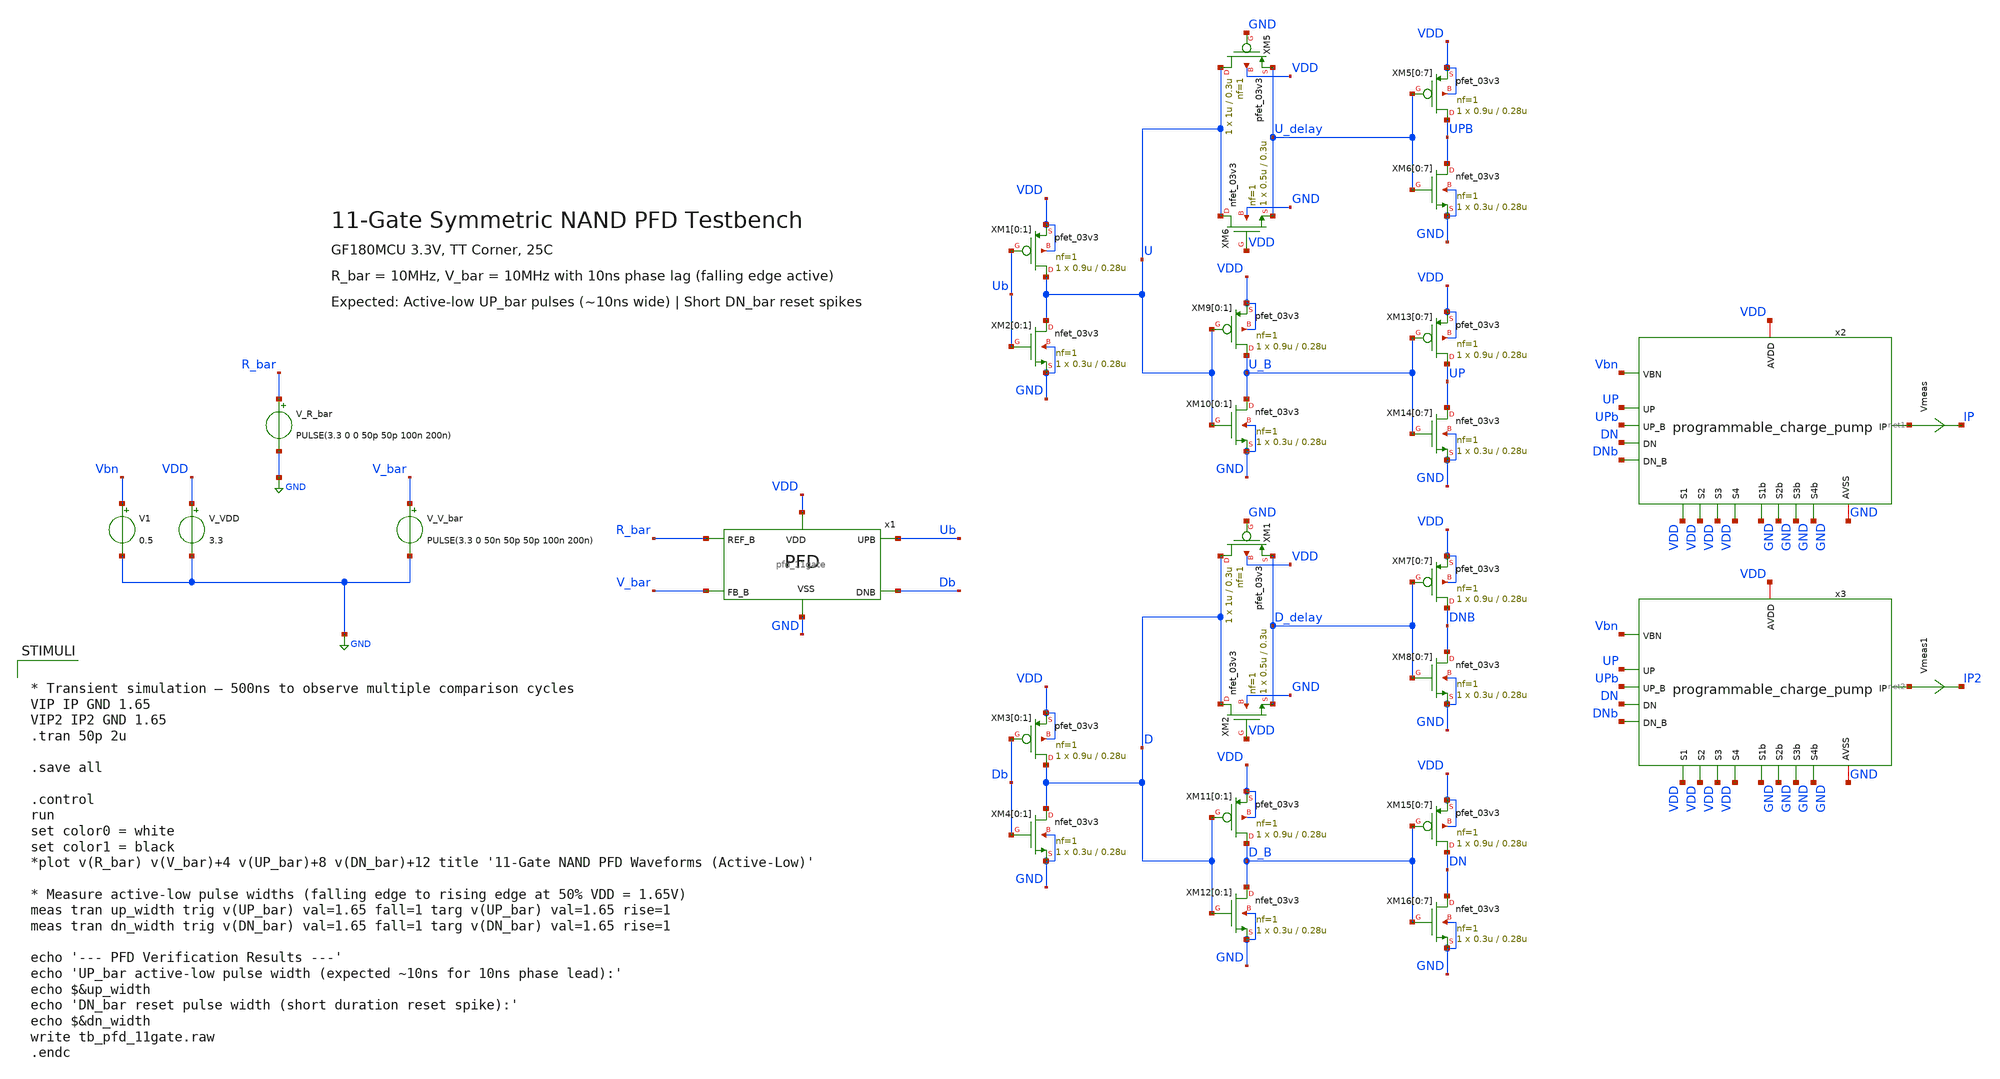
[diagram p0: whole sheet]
** sch_path: designs/libs/tb_analog/tb_pfd/tb_pfd_11gate.sch
**.subckt tb_pfd_11gate
V_R_bar R_bar GND PULSE(3.3 0 0 50p 50p 100n 200n)
V_V_bar V_bar GND PULSE(3.3 0 50n 50p 50p 100n 200n)
V_VDD VDD GND 3.3
x1 R_bar Ub Db V_bar VDD GND pfd_11gate
XM1[0] U Ub VDD VDD pfet_03v3 L=0.28u W=0.9u nf=1 ad='int((nf+1)/2) * W/nf * 0.18u' as='int((nf+2)/2) * W/nf * 0.18u'
+ pd='2*int((nf+1)/2) * (W/nf + 0.18u)' ps='2*int((nf+2)/2) * (W/nf + 0.18u)' nrd='0.18u / W' nrs='0.18u / W'
+ sa=0 sb=0 sd=0 m=1
XM1[1] U Ub VDD VDD pfet_03v3 L=0.28u W=0.9u nf=1 ad='int((nf+1)/2) * W/nf * 0.18u' as='int((nf+2)/2) * W/nf * 0.18u'
+ pd='2*int((nf+1)/2) * (W/nf + 0.18u)' ps='2*int((nf+2)/2) * (W/nf + 0.18u)' nrd='0.18u / W' nrs='0.18u / W'
+ sa=0 sb=0 sd=0 m=1
XM2[0] U Ub GND GND nfet_03v3 L=0.28u W=0.3u nf=1 ad='int((nf+1)/2) * W/nf * 0.18u' as='int((nf+2)/2) * W/nf * 0.18u'
+ pd='2*int((nf+1)/2) * (W/nf + 0.18u)' ps='2*int((nf+2)/2) * (W/nf + 0.18u)' nrd='0.18u / W' nrs='0.18u / W'
+ sa=0 sb=0 sd=0 m=1
XM2[1] U Ub GND GND nfet_03v3 L=0.28u W=0.3u nf=1 ad='int((nf+1)/2) * W/nf * 0.18u' as='int((nf+2)/2) * W/nf * 0.18u'
+ pd='2*int((nf+1)/2) * (W/nf + 0.18u)' ps='2*int((nf+2)/2) * (W/nf + 0.18u)' nrd='0.18u / W' nrs='0.18u / W'
+ sa=0 sb=0 sd=0 m=1
XM5 U GND U_delay VDD pfet_03v3 L=0.3u W=1u nf=1 ad='int((nf+1)/2) * W/nf * 0.18u' as='int((nf+2)/2) * W/nf * 0.18u'
+ pd='2*int((nf+1)/2) * (W/nf + 0.18u)' ps='2*int((nf+2)/2) * (W/nf + 0.18u)' nrd='0.18u / W' nrs='0.18u / W'
+ sa=0 sb=0 sd=0 m=1
XM6 U VDD U_delay GND nfet_03v3 L=0.3u W=0.5u nf=1 ad='int((nf+1)/2) * W/nf * 0.18u' as='int((nf+2)/2) * W/nf * 0.18u'
+ pd='2*int((nf+1)/2) * (W/nf + 0.18u)' ps='2*int((nf+2)/2) * (W/nf + 0.18u)' nrd='0.18u / W' nrs='0.18u / W'
+ sa=0 sb=0 sd=0 m=1
x2 GND VDD UP UPb DN net1 DNb Vbn GND VDD GND VDD GND VDD GND VDD programmable_charge_pump
V1 Vbn GND 0.5
Vmeas net1 IP 0
.save i(vmeas)
x3 GND VDD UP UPb DN net2 DNb Vbn GND VDD GND VDD GND VDD GND VDD programmable_charge_pump
Vmeas1 net2 IP2 0
.save i(vmeas1)
XM5[0] UPB U_delay VDD VDD pfet_03v3 L=0.28u W=0.9u nf=1 ad='int((nf+1)/2) * W/nf * 0.18u' as='int((nf+2)/2) * W/nf * 0.18u'
+ pd='2*int((nf+1)/2) * (W/nf + 0.18u)' ps='2*int((nf+2)/2) * (W/nf + 0.18u)' nrd='0.18u / W' nrs='0.18u / W'
+ sa=0 sb=0 sd=0 m=1
XM5[1] UPB U_delay VDD VDD pfet_03v3 L=0.28u W=0.9u nf=1 ad='int((nf+1)/2) * W/nf * 0.18u' as='int((nf+2)/2) * W/nf * 0.18u'
+ pd='2*int((nf+1)/2) * (W/nf + 0.18u)' ps='2*int((nf+2)/2) * (W/nf + 0.18u)' nrd='0.18u / W' nrs='0.18u / W'
+ sa=0 sb=0 sd=0 m=1
XM5[2] UPB U_delay VDD VDD pfet_03v3 L=0.28u W=0.9u nf=1 ad='int((nf+1)/2) * W/nf * 0.18u' as='int((nf+2)/2) * W/nf * 0.18u'
+ pd='2*int((nf+1)/2) * (W/nf + 0.18u)' ps='2*int((nf+2)/2) * (W/nf + 0.18u)' nrd='0.18u / W' nrs='0.18u / W'
+ sa=0 sb=0 sd=0 m=1
XM5[3] UPB U_delay VDD VDD pfet_03v3 L=0.28u W=0.9u nf=1 ad='int((nf+1)/2) * W/nf * 0.18u' as='int((nf+2)/2) * W/nf * 0.18u'
+ pd='2*int((nf+1)/2) * (W/nf + 0.18u)' ps='2*int((nf+2)/2) * (W/nf + 0.18u)' nrd='0.18u / W' nrs='0.18u / W'
+ sa=0 sb=0 sd=0 m=1
XM5[4] UPB U_delay VDD VDD pfet_03v3 L=0.28u W=0.9u nf=1 ad='int((nf+1)/2) * W/nf * 0.18u' as='int((nf+2)/2) * W/nf * 0.18u'
+ pd='2*int((nf+1)/2) * (W/nf + 0.18u)' ps='2*int((nf+2)/2) * (W/nf + 0.18u)' nrd='0.18u / W' nrs='0.18u / W'
+ sa=0 sb=0 sd=0 m=1
XM5[5] UPB U_delay VDD VDD pfet_03v3 L=0.28u W=0.9u nf=1 ad='int((nf+1)/2) * W/nf * 0.18u' as='int((nf+2)/2) * W/nf * 0.18u'
+ pd='2*int((nf+1)/2) * (W/nf + 0.18u)' ps='2*int((nf+2)/2) * (W/nf + 0.18u)' nrd='0.18u / W' nrs='0.18u / W'
+ sa=0 sb=0 sd=0 m=1
XM5[6] UPB U_delay VDD VDD pfet_03v3 L=0.28u W=0.9u nf=1 ad='int((nf+1)/2) * W/nf * 0.18u' as='int((nf+2)/2) * W/nf * 0.18u'
+ pd='2*int((nf+1)/2) * (W/nf + 0.18u)' ps='2*int((nf+2)/2) * (W/nf + 0.18u)' nrd='0.18u / W' nrs='0.18u / W'
+ sa=0 sb=0 sd=0 m=1
XM5[7] UPB U_delay VDD VDD pfet_03v3 L=0.28u W=0.9u nf=1 ad='int((nf+1)/2) * W/nf * 0.18u' as='int((nf+2)/2) * W/nf * 0.18u'
+ pd='2*int((nf+1)/2) * (W/nf + 0.18u)' ps='2*int((nf+2)/2) * (W/nf + 0.18u)' nrd='0.18u / W' nrs='0.18u / W'
+ sa=0 sb=0 sd=0 m=1
XM6[0] UPB U_delay GND GND nfet_03v3 L=0.28u W=0.3u nf=1 ad='int((nf+1)/2) * W/nf * 0.18u' as='int((nf+2)/2) * W/nf * 0.18u'
+ pd='2*int((nf+1)/2) * (W/nf + 0.18u)' ps='2*int((nf+2)/2) * (W/nf + 0.18u)' nrd='0.18u / W' nrs='0.18u / W'
+ sa=0 sb=0 sd=0 m=1
XM6[1] UPB U_delay GND GND nfet_03v3 L=0.28u W=0.3u nf=1 ad='int((nf+1)/2) * W/nf * 0.18u' as='int((nf+2)/2) * W/nf * 0.18u'
+ pd='2*int((nf+1)/2) * (W/nf + 0.18u)' ps='2*int((nf+2)/2) * (W/nf + 0.18u)' nrd='0.18u / W' nrs='0.18u / W'
+ sa=0 sb=0 sd=0 m=1
XM6[2] UPB U_delay GND GND nfet_03v3 L=0.28u W=0.3u nf=1 ad='int((nf+1)/2) * W/nf * 0.18u' as='int((nf+2)/2) * W/nf * 0.18u'
+ pd='2*int((nf+1)/2) * (W/nf + 0.18u)' ps='2*int((nf+2)/2) * (W/nf + 0.18u)' nrd='0.18u / W' nrs='0.18u / W'
+ sa=0 sb=0 sd=0 m=1
XM6[3] UPB U_delay GND GND nfet_03v3 L=0.28u W=0.3u nf=1 ad='int((nf+1)/2) * W/nf * 0.18u' as='int((nf+2)/2) * W/nf * 0.18u'
+ pd='2*int((nf+1)/2) * (W/nf + 0.18u)' ps='2*int((nf+2)/2) * (W/nf + 0.18u)' nrd='0.18u / W' nrs='0.18u / W'
+ sa=0 sb=0 sd=0 m=1
XM6[4] UPB U_delay GND GND nfet_03v3 L=0.28u W=0.3u nf=1 ad='int((nf+1)/2) * W/nf * 0.18u' as='int((nf+2)/2) * W/nf * 0.18u'
+ pd='2*int((nf+1)/2) * (W/nf + 0.18u)' ps='2*int((nf+2)/2) * (W/nf + 0.18u)' nrd='0.18u / W' nrs='0.18u / W'
+ sa=0 sb=0 sd=0 m=1
XM6[5] UPB U_delay GND GND nfet_03v3 L=0.28u W=0.3u nf=1 ad='int((nf+1)/2) * W/nf * 0.18u' as='int((nf+2)/2) * W/nf * 0.18u'
+ pd='2*int((nf+1)/2) * (W/nf + 0.18u)' ps='2*int((nf+2)/2) * (W/nf + 0.18u)' nrd='0.18u / W' nrs='0.18u / W'
+ sa=0 sb=0 sd=0 m=1
XM6[6] UPB U_delay GND GND nfet_03v3 L=0.28u W=0.3u nf=1 ad='int((nf+1)/2) * W/nf * 0.18u' as='int((nf+2)/2) * W/nf * 0.18u'
+ pd='2*int((nf+1)/2) * (W/nf + 0.18u)' ps='2*int((nf+2)/2) * (W/nf + 0.18u)' nrd='0.18u / W' nrs='0.18u / W'
+ sa=0 sb=0 sd=0 m=1
XM6[7] UPB U_delay GND GND nfet_03v3 L=0.28u W=0.3u nf=1 ad='int((nf+1)/2) * W/nf * 0.18u' as='int((nf+2)/2) * W/nf * 0.18u'
+ pd='2*int((nf+1)/2) * (W/nf + 0.18u)' ps='2*int((nf+2)/2) * (W/nf + 0.18u)' nrd='0.18u / W' nrs='0.18u / W'
+ sa=0 sb=0 sd=0 m=1
XM9[0] U_B U VDD VDD pfet_03v3 L=0.28u W=0.9u nf=1 ad='int((nf+1)/2) * W/nf * 0.18u' as='int((nf+2)/2) * W/nf * 0.18u'
+ pd='2*int((nf+1)/2) * (W/nf + 0.18u)' ps='2*int((nf+2)/2) * (W/nf + 0.18u)' nrd='0.18u / W' nrs='0.18u / W'
+ sa=0 sb=0 sd=0 m=1
XM9[1] U_B U VDD VDD pfet_03v3 L=0.28u W=0.9u nf=1 ad='int((nf+1)/2) * W/nf * 0.18u' as='int((nf+2)/2) * W/nf * 0.18u'
+ pd='2*int((nf+1)/2) * (W/nf + 0.18u)' ps='2*int((nf+2)/2) * (W/nf + 0.18u)' nrd='0.18u / W' nrs='0.18u / W'
+ sa=0 sb=0 sd=0 m=1
XM10[0] U_B U GND GND nfet_03v3 L=0.28u W=0.3u nf=1 ad='int((nf+1)/2) * W/nf * 0.18u' as='int((nf+2)/2) * W/nf * 0.18u'
+ pd='2*int((nf+1)/2) * (W/nf + 0.18u)' ps='2*int((nf+2)/2) * (W/nf + 0.18u)' nrd='0.18u / W' nrs='0.18u / W'
+ sa=0 sb=0 sd=0 m=1
XM10[1] U_B U GND GND nfet_03v3 L=0.28u W=0.3u nf=1 ad='int((nf+1)/2) * W/nf * 0.18u' as='int((nf+2)/2) * W/nf * 0.18u'
+ pd='2*int((nf+1)/2) * (W/nf + 0.18u)' ps='2*int((nf+2)/2) * (W/nf + 0.18u)' nrd='0.18u / W' nrs='0.18u / W'
+ sa=0 sb=0 sd=0 m=1
XM13[0] UP U_B VDD VDD pfet_03v3 L=0.28u W=0.9u nf=1 ad='int((nf+1)/2) * W/nf * 0.18u' as='int((nf+2)/2) * W/nf * 0.18u'
+ pd='2*int((nf+1)/2) * (W/nf + 0.18u)' ps='2*int((nf+2)/2) * (W/nf + 0.18u)' nrd='0.18u / W' nrs='0.18u / W'
+ sa=0 sb=0 sd=0 m=1
XM13[1] UP U_B VDD VDD pfet_03v3 L=0.28u W=0.9u nf=1 ad='int((nf+1)/2) * W/nf * 0.18u' as='int((nf+2)/2) * W/nf * 0.18u'
+ pd='2*int((nf+1)/2) * (W/nf + 0.18u)' ps='2*int((nf+2)/2) * (W/nf + 0.18u)' nrd='0.18u / W' nrs='0.18u / W'
+ sa=0 sb=0 sd=0 m=1
XM13[2] UP U_B VDD VDD pfet_03v3 L=0.28u W=0.9u nf=1 ad='int((nf+1)/2) * W/nf * 0.18u' as='int((nf+2)/2) * W/nf * 0.18u'
+ pd='2*int((nf+1)/2) * (W/nf + 0.18u)' ps='2*int((nf+2)/2) * (W/nf + 0.18u)' nrd='0.18u / W' nrs='0.18u / W'
+ sa=0 sb=0 sd=0 m=1
XM13[3] UP U_B VDD VDD pfet_03v3 L=0.28u W=0.9u nf=1 ad='int((nf+1)/2) * W/nf * 0.18u' as='int((nf+2)/2) * W/nf * 0.18u'
+ pd='2*int((nf+1)/2) * (W/nf + 0.18u)' ps='2*int((nf+2)/2) * (W/nf + 0.18u)' nrd='0.18u / W' nrs='0.18u / W'
+ sa=0 sb=0 sd=0 m=1
XM13[4] UP U_B VDD VDD pfet_03v3 L=0.28u W=0.9u nf=1 ad='int((nf+1)/2) * W/nf * 0.18u' as='int((nf+2)/2) * W/nf * 0.18u'
+ pd='2*int((nf+1)/2) * (W/nf + 0.18u)' ps='2*int((nf+2)/2) * (W/nf + 0.18u)' nrd='0.18u / W' nrs='0.18u / W'
+ sa=0 sb=0 sd=0 m=1
XM13[5] UP U_B VDD VDD pfet_03v3 L=0.28u W=0.9u nf=1 ad='int((nf+1)/2) * W/nf * 0.18u' as='int((nf+2)/2) * W/nf * 0.18u'
+ pd='2*int((nf+1)/2) * (W/nf + 0.18u)' ps='2*int((nf+2)/2) * (W/nf + 0.18u)' nrd='0.18u / W' nrs='0.18u / W'
+ sa=0 sb=0 sd=0 m=1
XM13[6] UP U_B VDD VDD pfet_03v3 L=0.28u W=0.9u nf=1 ad='int((nf+1)/2) * W/nf * 0.18u' as='int((nf+2)/2) * W/nf * 0.18u'
+ pd='2*int((nf+1)/2) * (W/nf + 0.18u)' ps='2*int((nf+2)/2) * (W/nf + 0.18u)' nrd='0.18u / W' nrs='0.18u / W'
+ sa=0 sb=0 sd=0 m=1
XM13[7] UP U_B VDD VDD pfet_03v3 L=0.28u W=0.9u nf=1 ad='int((nf+1)/2) * W/nf * 0.18u' as='int((nf+2)/2) * W/nf * 0.18u'
+ pd='2*int((nf+1)/2) * (W/nf + 0.18u)' ps='2*int((nf+2)/2) * (W/nf + 0.18u)' nrd='0.18u / W' nrs='0.18u / W'
+ sa=0 sb=0 sd=0 m=1
XM14[0] UP U_B GND GND nfet_03v3 L=0.28u W=0.3u nf=1 ad='int((nf+1)/2) * W/nf * 0.18u' as='int((nf+2)/2) * W/nf * 0.18u'
+ pd='2*int((nf+1)/2) * (W/nf + 0.18u)' ps='2*int((nf+2)/2) * (W/nf + 0.18u)' nrd='0.18u / W' nrs='0.18u / W'
+ sa=0 sb=0 sd=0 m=1
XM14[1] UP U_B GND GND nfet_03v3 L=0.28u W=0.3u nf=1 ad='int((nf+1)/2) * W/nf * 0.18u' as='int((nf+2)/2) * W/nf * 0.18u'
+ pd='2*int((nf+1)/2) * (W/nf + 0.18u)' ps='2*int((nf+2)/2) * (W/nf + 0.18u)' nrd='0.18u / W' nrs='0.18u / W'
+ sa=0 sb=0 sd=0 m=1
XM14[2] UP U_B GND GND nfet_03v3 L=0.28u W=0.3u nf=1 ad='int((nf+1)/2) * W/nf * 0.18u' as='int((nf+2)/2) * W/nf * 0.18u'
+ pd='2*int((nf+1)/2) * (W/nf + 0.18u)' ps='2*int((nf+2)/2) * (W/nf + 0.18u)' nrd='0.18u / W' nrs='0.18u / W'
+ sa=0 sb=0 sd=0 m=1
XM14[3] UP U_B GND GND nfet_03v3 L=0.28u W=0.3u nf=1 ad='int((nf+1)/2) * W/nf * 0.18u' as='int((nf+2)/2) * W/nf * 0.18u'
+ pd='2*int((nf+1)/2) * (W/nf + 0.18u)' ps='2*int((nf+2)/2) * (W/nf + 0.18u)' nrd='0.18u / W' nrs='0.18u / W'
+ sa=0 sb=0 sd=0 m=1
XM14[4] UP U_B GND GND nfet_03v3 L=0.28u W=0.3u nf=1 ad='int((nf+1)/2) * W/nf * 0.18u' as='int((nf+2)/2) * W/nf * 0.18u'
+ pd='2*int((nf+1)/2) * (W/nf + 0.18u)' ps='2*int((nf+2)/2) * (W/nf + 0.18u)' nrd='0.18u / W' nrs='0.18u / W'
+ sa=0 sb=0 sd=0 m=1
XM14[5] UP U_B GND GND nfet_03v3 L=0.28u W=0.3u nf=1 ad='int((nf+1)/2) * W/nf * 0.18u' as='int((nf+2)/2) * W/nf * 0.18u'
+ pd='2*int((nf+1)/2) * (W/nf + 0.18u)' ps='2*int((nf+2)/2) * (W/nf + 0.18u)' nrd='0.18u / W' nrs='0.18u / W'
+ sa=0 sb=0 sd=0 m=1
XM14[6] UP U_B GND GND nfet_03v3 L=0.28u W=0.3u nf=1 ad='int((nf+1)/2) * W/nf * 0.18u' as='int((nf+2)/2) * W/nf * 0.18u'
+ pd='2*int((nf+1)/2) * (W/nf + 0.18u)' ps='2*int((nf+2)/2) * (W/nf + 0.18u)' nrd='0.18u / W' nrs='0.18u / W'
+ sa=0 sb=0 sd=0 m=1
XM14[7] UP U_B GND GND nfet_03v3 L=0.28u W=0.3u nf=1 ad='int((nf+1)/2) * W/nf * 0.18u' as='int((nf+2)/2) * W/nf * 0.18u'
+ pd='2*int((nf+1)/2) * (W/nf + 0.18u)' ps='2*int((nf+2)/2) * (W/nf + 0.18u)' nrd='0.18u / W' nrs='0.18u / W'
+ sa=0 sb=0 sd=0 m=1
XM3[0] D Db VDD VDD pfet_03v3 L=0.28u W=0.9u nf=1 ad='int((nf+1)/2) * W/nf * 0.18u' as='int((nf+2)/2) * W/nf * 0.18u'
+ pd='2*int((nf+1)/2) * (W/nf + 0.18u)' ps='2*int((nf+2)/2) * (W/nf + 0.18u)' nrd='0.18u / W' nrs='0.18u / W'
+ sa=0 sb=0 sd=0 m=1
XM3[1] D Db VDD VDD pfet_03v3 L=0.28u W=0.9u nf=1 ad='int((nf+1)/2) * W/nf * 0.18u' as='int((nf+2)/2) * W/nf * 0.18u'
+ pd='2*int((nf+1)/2) * (W/nf + 0.18u)' ps='2*int((nf+2)/2) * (W/nf + 0.18u)' nrd='0.18u / W' nrs='0.18u / W'
+ sa=0 sb=0 sd=0 m=1
XM4[0] D Db GND GND nfet_03v3 L=0.28u W=0.3u nf=1 ad='int((nf+1)/2) * W/nf * 0.18u' as='int((nf+2)/2) * W/nf * 0.18u'
+ pd='2*int((nf+1)/2) * (W/nf + 0.18u)' ps='2*int((nf+2)/2) * (W/nf + 0.18u)' nrd='0.18u / W' nrs='0.18u / W'
+ sa=0 sb=0 sd=0 m=1
XM4[1] D Db GND GND nfet_03v3 L=0.28u W=0.3u nf=1 ad='int((nf+1)/2) * W/nf * 0.18u' as='int((nf+2)/2) * W/nf * 0.18u'
+ pd='2*int((nf+1)/2) * (W/nf + 0.18u)' ps='2*int((nf+2)/2) * (W/nf + 0.18u)' nrd='0.18u / W' nrs='0.18u / W'
+ sa=0 sb=0 sd=0 m=1
XM7[0] DNB D_delay VDD VDD pfet_03v3 L=0.28u W=0.9u nf=1 ad='int((nf+1)/2) * W/nf * 0.18u' as='int((nf+2)/2) * W/nf * 0.18u'
+ pd='2*int((nf+1)/2) * (W/nf + 0.18u)' ps='2*int((nf+2)/2) * (W/nf + 0.18u)' nrd='0.18u / W' nrs='0.18u / W'
+ sa=0 sb=0 sd=0 m=1
XM7[1] DNB D_delay VDD VDD pfet_03v3 L=0.28u W=0.9u nf=1 ad='int((nf+1)/2) * W/nf * 0.18u' as='int((nf+2)/2) * W/nf * 0.18u'
+ pd='2*int((nf+1)/2) * (W/nf + 0.18u)' ps='2*int((nf+2)/2) * (W/nf + 0.18u)' nrd='0.18u / W' nrs='0.18u / W'
+ sa=0 sb=0 sd=0 m=1
XM7[2] DNB D_delay VDD VDD pfet_03v3 L=0.28u W=0.9u nf=1 ad='int((nf+1)/2) * W/nf * 0.18u' as='int((nf+2)/2) * W/nf * 0.18u'
+ pd='2*int((nf+1)/2) * (W/nf + 0.18u)' ps='2*int((nf+2)/2) * (W/nf + 0.18u)' nrd='0.18u / W' nrs='0.18u / W'
+ sa=0 sb=0 sd=0 m=1
XM7[3] DNB D_delay VDD VDD pfet_03v3 L=0.28u W=0.9u nf=1 ad='int((nf+1)/2) * W/nf * 0.18u' as='int((nf+2)/2) * W/nf * 0.18u'
+ pd='2*int((nf+1)/2) * (W/nf + 0.18u)' ps='2*int((nf+2)/2) * (W/nf + 0.18u)' nrd='0.18u / W' nrs='0.18u / W'
+ sa=0 sb=0 sd=0 m=1
XM7[4] DNB D_delay VDD VDD pfet_03v3 L=0.28u W=0.9u nf=1 ad='int((nf+1)/2) * W/nf * 0.18u' as='int((nf+2)/2) * W/nf * 0.18u'
+ pd='2*int((nf+1)/2) * (W/nf + 0.18u)' ps='2*int((nf+2)/2) * (W/nf + 0.18u)' nrd='0.18u / W' nrs='0.18u / W'
+ sa=0 sb=0 sd=0 m=1
XM7[5] DNB D_delay VDD VDD pfet_03v3 L=0.28u W=0.9u nf=1 ad='int((nf+1)/2) * W/nf * 0.18u' as='int((nf+2)/2) * W/nf * 0.18u'
+ pd='2*int((nf+1)/2) * (W/nf + 0.18u)' ps='2*int((nf+2)/2) * (W/nf + 0.18u)' nrd='0.18u / W' nrs='0.18u / W'
+ sa=0 sb=0 sd=0 m=1
XM7[6] DNB D_delay VDD VDD pfet_03v3 L=0.28u W=0.9u nf=1 ad='int((nf+1)/2) * W/nf * 0.18u' as='int((nf+2)/2) * W/nf * 0.18u'
+ pd='2*int((nf+1)/2) * (W/nf + 0.18u)' ps='2*int((nf+2)/2) * (W/nf + 0.18u)' nrd='0.18u / W' nrs='0.18u / W'
+ sa=0 sb=0 sd=0 m=1
XM7[7] DNB D_delay VDD VDD pfet_03v3 L=0.28u W=0.9u nf=1 ad='int((nf+1)/2) * W/nf * 0.18u' as='int((nf+2)/2) * W/nf * 0.18u'
+ pd='2*int((nf+1)/2) * (W/nf + 0.18u)' ps='2*int((nf+2)/2) * (W/nf + 0.18u)' nrd='0.18u / W' nrs='0.18u / W'
+ sa=0 sb=0 sd=0 m=1
XM8[0] DNB D_delay GND GND nfet_03v3 L=0.28u W=0.3u nf=1 ad='int((nf+1)/2) * W/nf * 0.18u' as='int((nf+2)/2) * W/nf * 0.18u'
+ pd='2*int((nf+1)/2) * (W/nf + 0.18u)' ps='2*int((nf+2)/2) * (W/nf + 0.18u)' nrd='0.18u / W' nrs='0.18u / W'
+ sa=0 sb=0 sd=0 m=1
XM8[1] DNB D_delay GND GND nfet_03v3 L=0.28u W=0.3u nf=1 ad='int((nf+1)/2) * W/nf * 0.18u' as='int((nf+2)/2) * W/nf * 0.18u'
+ pd='2*int((nf+1)/2) * (W/nf + 0.18u)' ps='2*int((nf+2)/2) * (W/nf + 0.18u)' nrd='0.18u / W' nrs='0.18u / W'
+ sa=0 sb=0 sd=0 m=1
XM8[2] DNB D_delay GND GND nfet_03v3 L=0.28u W=0.3u nf=1 ad='int((nf+1)/2) * W/nf * 0.18u' as='int((nf+2)/2) * W/nf * 0.18u'
+ pd='2*int((nf+1)/2) * (W/nf + 0.18u)' ps='2*int((nf+2)/2) * (W/nf + 0.18u)' nrd='0.18u / W' nrs='0.18u / W'
+ sa=0 sb=0 sd=0 m=1
XM8[3] DNB D_delay GND GND nfet_03v3 L=0.28u W=0.3u nf=1 ad='int((nf+1)/2) * W/nf * 0.18u' as='int((nf+2)/2) * W/nf * 0.18u'
+ pd='2*int((nf+1)/2) * (W/nf + 0.18u)' ps='2*int((nf+2)/2) * (W/nf + 0.18u)' nrd='0.18u / W' nrs='0.18u / W'
+ sa=0 sb=0 sd=0 m=1
XM8[4] DNB D_delay GND GND nfet_03v3 L=0.28u W=0.3u nf=1 ad='int((nf+1)/2) * W/nf * 0.18u' as='int((nf+2)/2) * W/nf * 0.18u'
+ pd='2*int((nf+1)/2) * (W/nf + 0.18u)' ps='2*int((nf+2)/2) * (W/nf + 0.18u)' nrd='0.18u / W' nrs='0.18u / W'
+ sa=0 sb=0 sd=0 m=1
XM8[5] DNB D_delay GND GND nfet_03v3 L=0.28u W=0.3u nf=1 ad='int((nf+1)/2) * W/nf * 0.18u' as='int((nf+2)/2) * W/nf * 0.18u'
+ pd='2*int((nf+1)/2) * (W/nf + 0.18u)' ps='2*int((nf+2)/2) * (W/nf + 0.18u)' nrd='0.18u / W' nrs='0.18u / W'
+ sa=0 sb=0 sd=0 m=1
XM8[6] DNB D_delay GND GND nfet_03v3 L=0.28u W=0.3u nf=1 ad='int((nf+1)/2) * W/nf * 0.18u' as='int((nf+2)/2) * W/nf * 0.18u'
+ pd='2*int((nf+1)/2) * (W/nf + 0.18u)' ps='2*int((nf+2)/2) * (W/nf + 0.18u)' nrd='0.18u / W' nrs='0.18u / W'
+ sa=0 sb=0 sd=0 m=1
XM8[7] DNB D_delay GND GND nfet_03v3 L=0.28u W=0.3u nf=1 ad='int((nf+1)/2) * W/nf * 0.18u' as='int((nf+2)/2) * W/nf * 0.18u'
+ pd='2*int((nf+1)/2) * (W/nf + 0.18u)' ps='2*int((nf+2)/2) * (W/nf + 0.18u)' nrd='0.18u / W' nrs='0.18u / W'
+ sa=0 sb=0 sd=0 m=1
XM11[0] D_B D VDD VDD pfet_03v3 L=0.28u W=0.9u nf=1 ad='int((nf+1)/2) * W/nf * 0.18u' as='int((nf+2)/2) * W/nf * 0.18u'
+ pd='2*int((nf+1)/2) * (W/nf + 0.18u)' ps='2*int((nf+2)/2) * (W/nf + 0.18u)' nrd='0.18u / W' nrs='0.18u / W'
+ sa=0 sb=0 sd=0 m=1
XM11[1] D_B D VDD VDD pfet_03v3 L=0.28u W=0.9u nf=1 ad='int((nf+1)/2) * W/nf * 0.18u' as='int((nf+2)/2) * W/nf * 0.18u'
+ pd='2*int((nf+1)/2) * (W/nf + 0.18u)' ps='2*int((nf+2)/2) * (W/nf + 0.18u)' nrd='0.18u / W' nrs='0.18u / W'
+ sa=0 sb=0 sd=0 m=1
XM12[0] D_B D GND GND nfet_03v3 L=0.28u W=0.3u nf=1 ad='int((nf+1)/2) * W/nf * 0.18u' as='int((nf+2)/2) * W/nf * 0.18u'
+ pd='2*int((nf+1)/2) * (W/nf + 0.18u)' ps='2*int((nf+2)/2) * (W/nf + 0.18u)' nrd='0.18u / W' nrs='0.18u / W'
+ sa=0 sb=0 sd=0 m=1
XM12[1] D_B D GND GND nfet_03v3 L=0.28u W=0.3u nf=1 ad='int((nf+1)/2) * W/nf * 0.18u' as='int((nf+2)/2) * W/nf * 0.18u'
+ pd='2*int((nf+1)/2) * (W/nf + 0.18u)' ps='2*int((nf+2)/2) * (W/nf + 0.18u)' nrd='0.18u / W' nrs='0.18u / W'
+ sa=0 sb=0 sd=0 m=1
XM15[0] DN D_B VDD VDD pfet_03v3 L=0.28u W=0.9u nf=1 ad='int((nf+1)/2) * W/nf * 0.18u' as='int((nf+2)/2) * W/nf * 0.18u'
+ pd='2*int((nf+1)/2) * (W/nf + 0.18u)' ps='2*int((nf+2)/2) * (W/nf + 0.18u)' nrd='0.18u / W' nrs='0.18u / W'
+ sa=0 sb=0 sd=0 m=1
XM15[1] DN D_B VDD VDD pfet_03v3 L=0.28u W=0.9u nf=1 ad='int((nf+1)/2) * W/nf * 0.18u' as='int((nf+2)/2) * W/nf * 0.18u'
+ pd='2*int((nf+1)/2) * (W/nf + 0.18u)' ps='2*int((nf+2)/2) * (W/nf + 0.18u)' nrd='0.18u / W' nrs='0.18u / W'
+ sa=0 sb=0 sd=0 m=1
XM15[2] DN D_B VDD VDD pfet_03v3 L=0.28u W=0.9u nf=1 ad='int((nf+1)/2) * W/nf * 0.18u' as='int((nf+2)/2) * W/nf * 0.18u'
+ pd='2*int((nf+1)/2) * (W/nf + 0.18u)' ps='2*int((nf+2)/2) * (W/nf + 0.18u)' nrd='0.18u / W' nrs='0.18u / W'
+ sa=0 sb=0 sd=0 m=1
XM15[3] DN D_B VDD VDD pfet_03v3 L=0.28u W=0.9u nf=1 ad='int((nf+1)/2) * W/nf * 0.18u' as='int((nf+2)/2) * W/nf * 0.18u'
+ pd='2*int((nf+1)/2) * (W/nf + 0.18u)' ps='2*int((nf+2)/2) * (W/nf + 0.18u)' nrd='0.18u / W' nrs='0.18u / W'
+ sa=0 sb=0 sd=0 m=1
XM15[4] DN D_B VDD VDD pfet_03v3 L=0.28u W=0.9u nf=1 ad='int((nf+1)/2) * W/nf * 0.18u' as='int((nf+2)/2) * W/nf * 0.18u'
+ pd='2*int((nf+1)/2) * (W/nf + 0.18u)' ps='2*int((nf+2)/2) * (W/nf + 0.18u)' nrd='0.18u / W' nrs='0.18u / W'
+ sa=0 sb=0 sd=0 m=1
XM15[5] DN D_B VDD VDD pfet_03v3 L=0.28u W=0.9u nf=1 ad='int((nf+1)/2) * W/nf * 0.18u' as='int((nf+2)/2) * W/nf * 0.18u'
+ pd='2*int((nf+1)/2) * (W/nf + 0.18u)' ps='2*int((nf+2)/2) * (W/nf + 0.18u)' nrd='0.18u / W' nrs='0.18u / W'
+ sa=0 sb=0 sd=0 m=1
XM15[6] DN D_B VDD VDD pfet_03v3 L=0.28u W=0.9u nf=1 ad='int((nf+1)/2) * W/nf * 0.18u' as='int((nf+2)/2) * W/nf * 0.18u'
+ pd='2*int((nf+1)/2) * (W/nf + 0.18u)' ps='2*int((nf+2)/2) * (W/nf + 0.18u)' nrd='0.18u / W' nrs='0.18u / W'
+ sa=0 sb=0 sd=0 m=1
XM15[7] DN D_B VDD VDD pfet_03v3 L=0.28u W=0.9u nf=1 ad='int((nf+1)/2) * W/nf * 0.18u' as='int((nf+2)/2) * W/nf * 0.18u'
+ pd='2*int((nf+1)/2) * (W/nf + 0.18u)' ps='2*int((nf+2)/2) * (W/nf + 0.18u)' nrd='0.18u / W' nrs='0.18u / W'
+ sa=0 sb=0 sd=0 m=1
XM16[0] DN D_B GND GND nfet_03v3 L=0.28u W=0.3u nf=1 ad='int((nf+1)/2) * W/nf * 0.18u' as='int((nf+2)/2) * W/nf * 0.18u'
+ pd='2*int((nf+1)/2) * (W/nf + 0.18u)' ps='2*int((nf+2)/2) * (W/nf + 0.18u)' nrd='0.18u / W' nrs='0.18u / W'
+ sa=0 sb=0 sd=0 m=1
XM16[1] DN D_B GND GND nfet_03v3 L=0.28u W=0.3u nf=1 ad='int((nf+1)/2) * W/nf * 0.18u' as='int((nf+2)/2) * W/nf * 0.18u'
+ pd='2*int((nf+1)/2) * (W/nf + 0.18u)' ps='2*int((nf+2)/2) * (W/nf + 0.18u)' nrd='0.18u / W' nrs='0.18u / W'
+ sa=0 sb=0 sd=0 m=1
XM16[2] DN D_B GND GND nfet_03v3 L=0.28u W=0.3u nf=1 ad='int((nf+1)/2) * W/nf * 0.18u' as='int((nf+2)/2) * W/nf * 0.18u'
+ pd='2*int((nf+1)/2) * (W/nf + 0.18u)' ps='2*int((nf+2)/2) * (W/nf + 0.18u)' nrd='0.18u / W' nrs='0.18u / W'
+ sa=0 sb=0 sd=0 m=1
XM16[3] DN D_B GND GND nfet_03v3 L=0.28u W=0.3u nf=1 ad='int((nf+1)/2) * W/nf * 0.18u' as='int((nf+2)/2) * W/nf * 0.18u'
+ pd='2*int((nf+1)/2) * (W/nf + 0.18u)' ps='2*int((nf+2)/2) * (W/nf + 0.18u)' nrd='0.18u / W' nrs='0.18u / W'
+ sa=0 sb=0 sd=0 m=1
XM16[4] DN D_B GND GND nfet_03v3 L=0.28u W=0.3u nf=1 ad='int((nf+1)/2) * W/nf * 0.18u' as='int((nf+2)/2) * W/nf * 0.18u'
+ pd='2*int((nf+1)/2) * (W/nf + 0.18u)' ps='2*int((nf+2)/2) * (W/nf + 0.18u)' nrd='0.18u / W' nrs='0.18u / W'
+ sa=0 sb=0 sd=0 m=1
XM16[5] DN D_B GND GND nfet_03v3 L=0.28u W=0.3u nf=1 ad='int((nf+1)/2) * W/nf * 0.18u' as='int((nf+2)/2) * W/nf * 0.18u'
+ pd='2*int((nf+1)/2) * (W/nf + 0.18u)' ps='2*int((nf+2)/2) * (W/nf + 0.18u)' nrd='0.18u / W' nrs='0.18u / W'
+ sa=0 sb=0 sd=0 m=1
XM16[6] DN D_B GND GND nfet_03v3 L=0.28u W=0.3u nf=1 ad='int((nf+1)/2) * W/nf * 0.18u' as='int((nf+2)/2) * W/nf * 0.18u'
+ pd='2*int((nf+1)/2) * (W/nf + 0.18u)' ps='2*int((nf+2)/2) * (W/nf + 0.18u)' nrd='0.18u / W' nrs='0.18u / W'
+ sa=0 sb=0 sd=0 m=1
XM16[7] DN D_B GND GND nfet_03v3 L=0.28u W=0.3u nf=1 ad='int((nf+1)/2) * W/nf * 0.18u' as='int((nf+2)/2) * W/nf * 0.18u'
+ pd='2*int((nf+1)/2) * (W/nf + 0.18u)' ps='2*int((nf+2)/2) * (W/nf + 0.18u)' nrd='0.18u / W' nrs='0.18u / W'
+ sa=0 sb=0 sd=0 m=1
XM1 D GND D_delay VDD pfet_03v3 L=0.3u W=1u nf=1 ad='int((nf+1)/2) * W/nf * 0.18u' as='int((nf+2)/2) * W/nf * 0.18u'
+ pd='2*int((nf+1)/2) * (W/nf + 0.18u)' ps='2*int((nf+2)/2) * (W/nf + 0.18u)' nrd='0.18u / W' nrs='0.18u / W'
+ sa=0 sb=0 sd=0 m=1
XM2 D VDD D_delay GND nfet_03v3 L=0.3u W=0.5u nf=1 ad='int((nf+1)/2) * W/nf * 0.18u' as='int((nf+2)/2) * W/nf * 0.18u'
+ pd='2*int((nf+1)/2) * (W/nf + 0.18u)' ps='2*int((nf+2)/2) * (W/nf + 0.18u)' nrd='0.18u / W' nrs='0.18u / W'
+ sa=0 sb=0 sd=0 m=1
**** begin user architecture code


* Transient simulation — 500ns to observe multiple comparison cycles
VIP IP GND 1.65
VIP2 IP2 GND 1.65
.tran 50p 2u

.save all

.control
run
set color0 = white
set color1 = black
*plot v(R_bar) v(V_bar)+4 v(UP_bar)+8 v(DN_bar)+12 title '11-Gate NAND PFD Waveforms (Active-Low)'

* Measure active-low pulse widths (falling edge to rising edge at 50% VDD = 1.65V)
meas tran up_width trig v(UP_bar) val=1.65 fall=1 targ v(UP_bar) val=1.65 rise=1
meas tran dn_width trig v(DN_bar) val=1.65 fall=1 targ v(DN_bar) val=1.65 rise=1

echo '--- PFD Verification Results ---'
echo 'UP_bar active-low pulse width (expected ~10ns for 10ns phase lead):'
echo $&up_width
echo 'DN_bar reset pulse width (short duration reset spike):'
echo $&dn_width
write tb_pfd_11gate.raw
.endc



.include /foss/pdks/ciel/gf180mcu/versions/7b70722e33c03fcb5dabcf4d479fb0822d9251c9/gf180mcuD/libs.ref/gf180mcu_fd_sc_mcu7t5v0/spice/gf180mcu_fd_sc_mcu7t5v0.spice
.include $::180MCU_MODELS/design.ngspice
.lib $::180MCU_MODELS/sm141064.ngspice typical

**** end user architecture code
**.ends
.GLOBAL GND
.end
